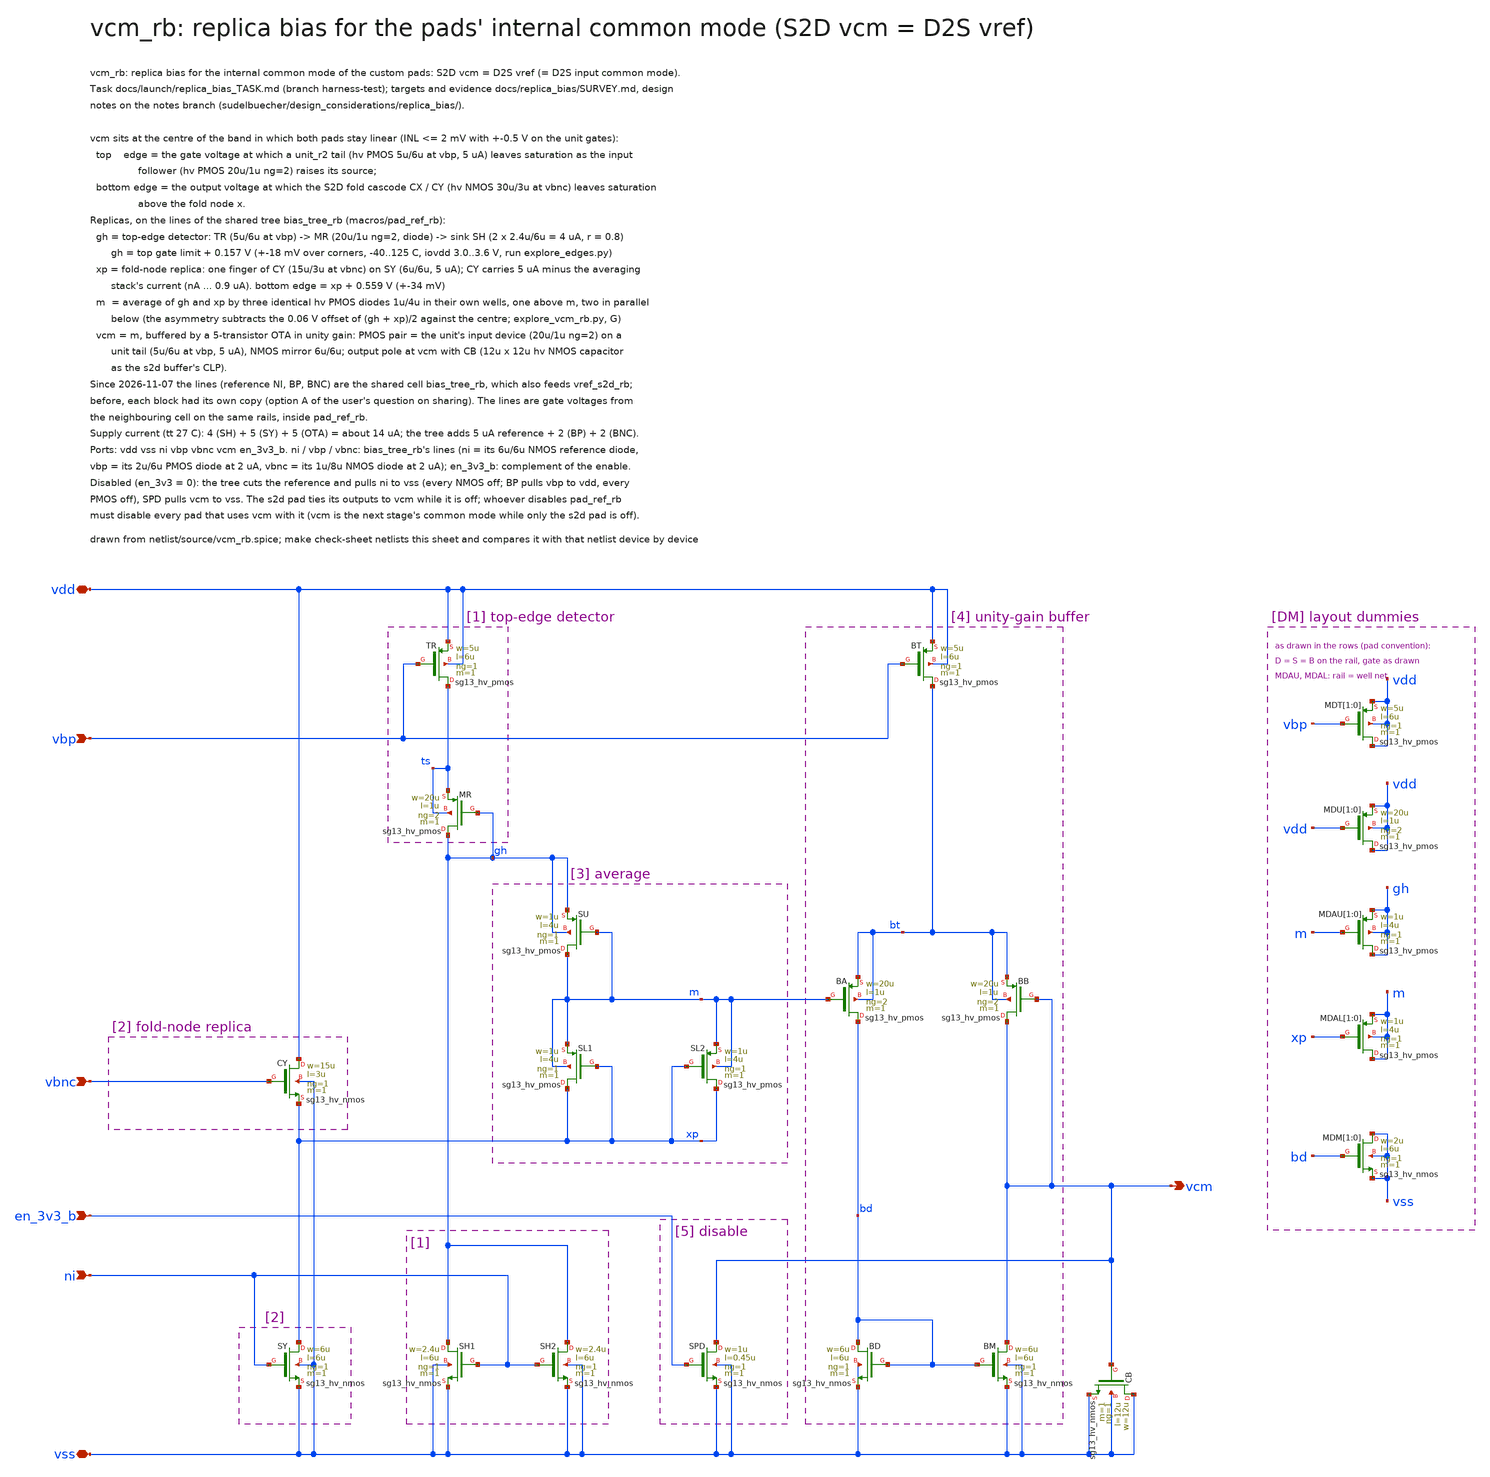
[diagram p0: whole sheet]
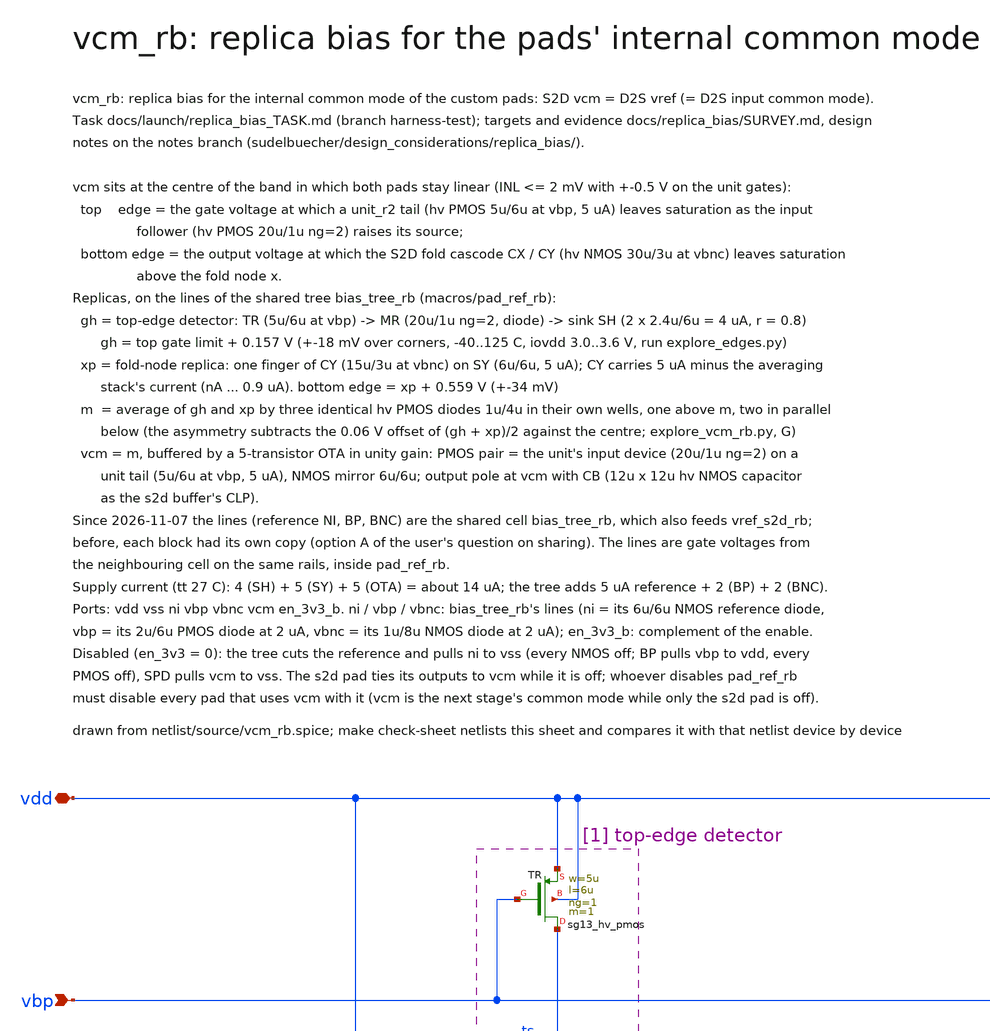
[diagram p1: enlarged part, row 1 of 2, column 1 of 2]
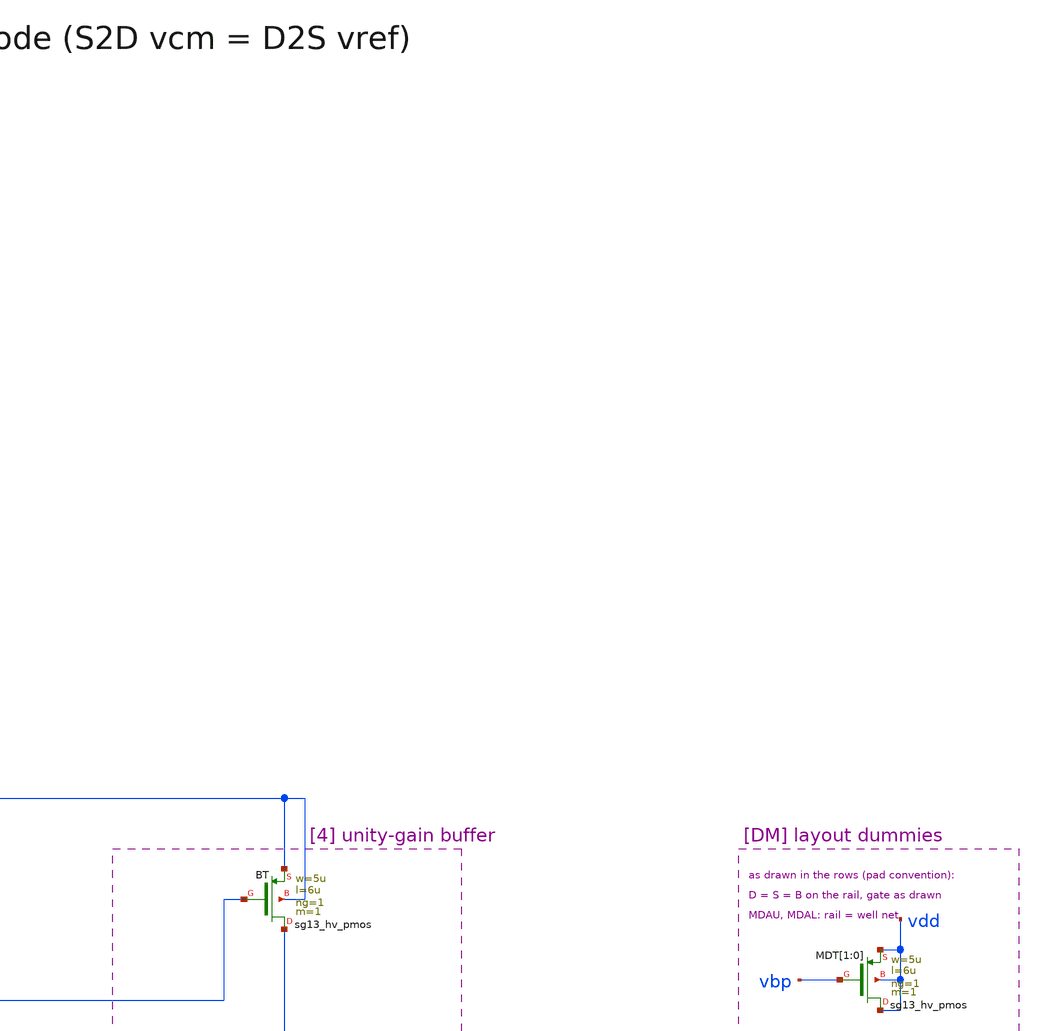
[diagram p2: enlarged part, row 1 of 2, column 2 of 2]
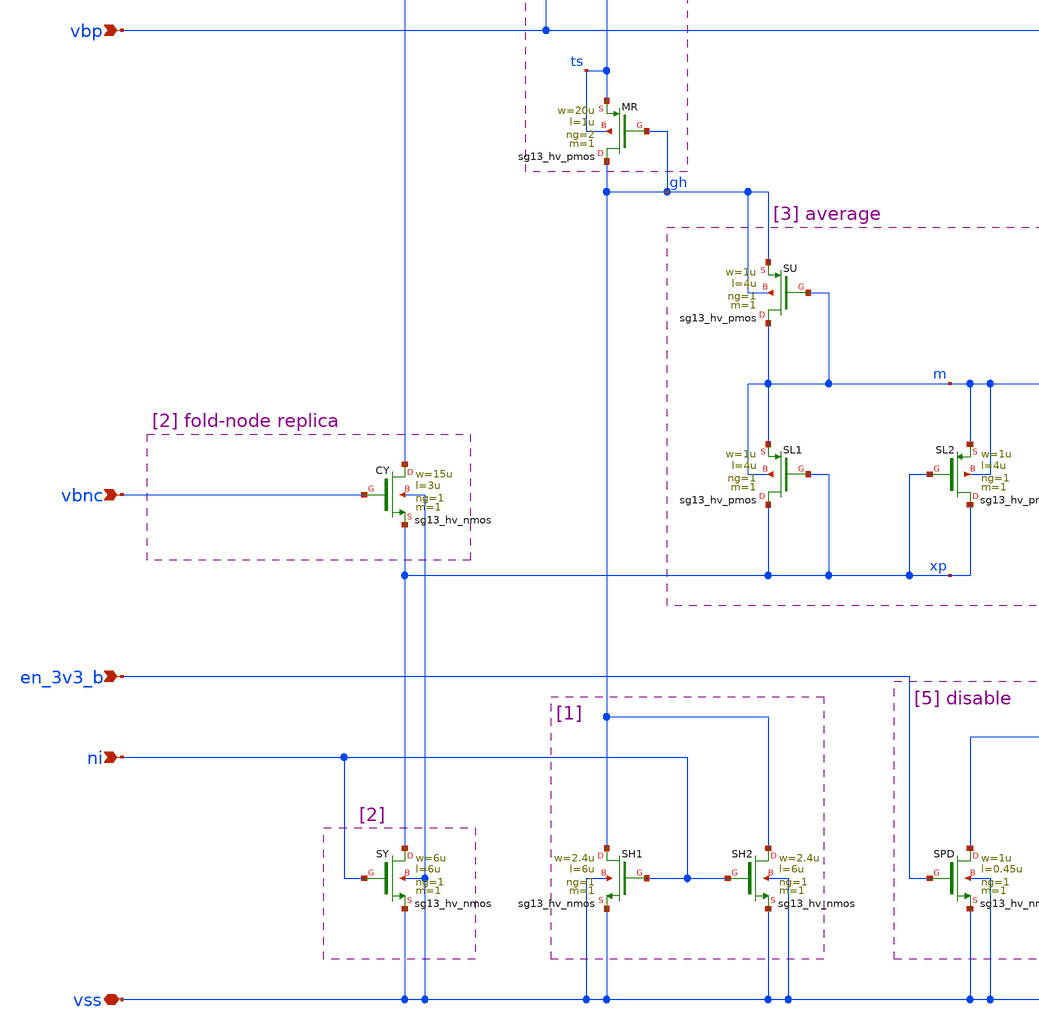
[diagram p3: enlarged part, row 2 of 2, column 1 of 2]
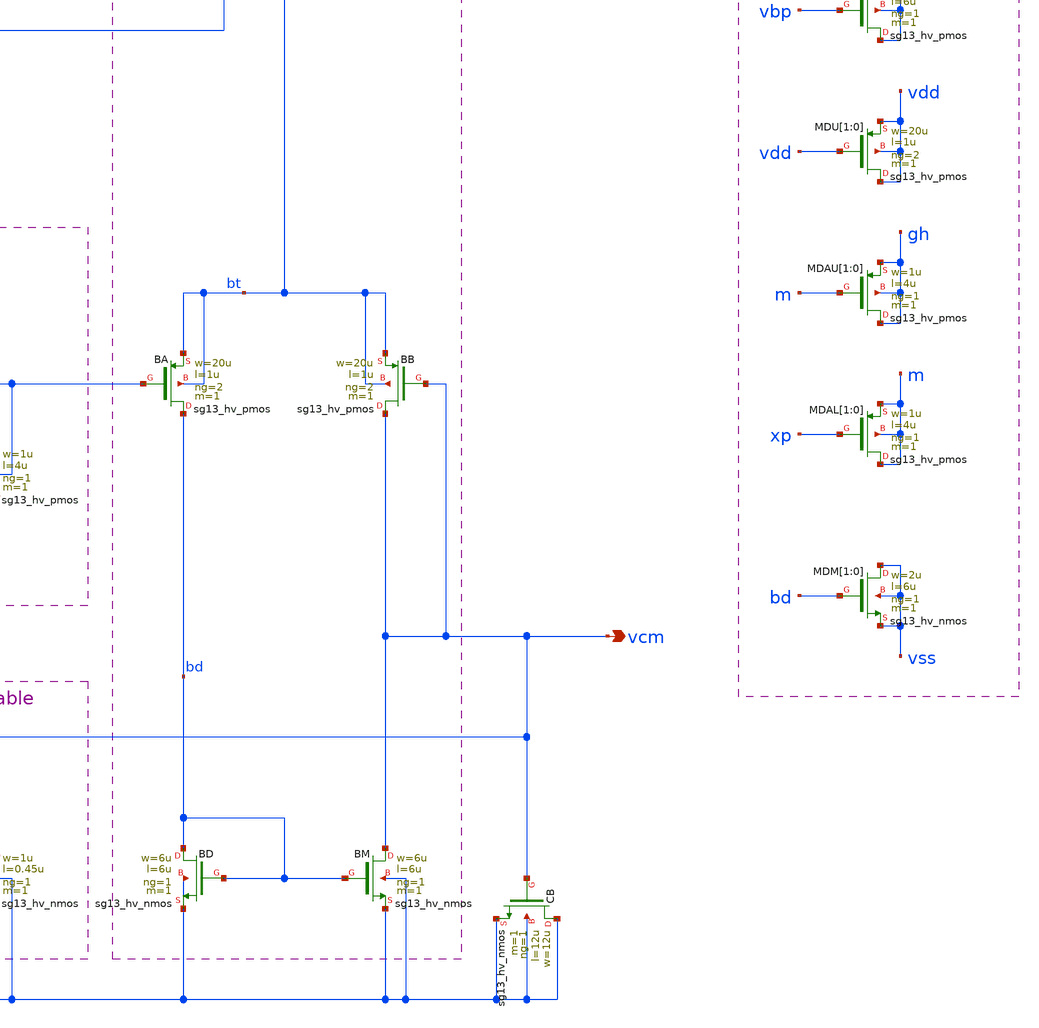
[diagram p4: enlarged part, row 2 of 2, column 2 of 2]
** sch_path: macros/vcm_rb/schematic/xschem/vcm_rb.sch
**.subckt vcm_rb vdd vss ni vbp vbnc vcm en_3v3_b
*.iopin vdd
*.iopin vss
*.ipin ni
*.ipin vbp
*.ipin vbnc
*.opin vcm
*.ipin en_3v3_b
XTR ts vbp vdd vdd sg13_hv_pmos w=5u l=6u ng=1 m=1 mm_ok=1
XMR gh gh ts ts sg13_hv_pmos w=20u l=1u ng=2 m=1 mm_ok=1
XSH1 gh ni vss vss sg13_hv_nmos w=2.4u l=6u ng=1 m=1 mm_ok=1
XSH2 gh ni vss vss sg13_hv_nmos w=2.4u l=6u ng=1 m=1 mm_ok=1
XCY vdd vbnc xp vss sg13_hv_nmos w=15u l=3u ng=1 m=1 mm_ok=1
XSY xp ni vss vss sg13_hv_nmos w=6u l=6u ng=1 m=1 mm_ok=1
XSU m m gh gh sg13_hv_pmos w=1u l=4u ng=1 m=1 mm_ok=1
XSL1 xp xp m m sg13_hv_pmos w=1u l=4u ng=1 m=1 mm_ok=1
XSL2 xp xp m m sg13_hv_pmos w=1u l=4u ng=1 m=1 mm_ok=1
XBT bt vbp vdd vdd sg13_hv_pmos w=5u l=6u ng=1 m=1 mm_ok=1
XBA bd m bt bt sg13_hv_pmos w=20u l=1u ng=2 m=1 mm_ok=1
XBB vcm vcm bt bt sg13_hv_pmos w=20u l=1u ng=2 m=1 mm_ok=1
XBD bd bd vss vss sg13_hv_nmos w=6u l=6u ng=1 m=1 mm_ok=1
XBM vcm bd vss vss sg13_hv_nmos w=6u l=6u ng=1 m=1 mm_ok=1
XCB vss vcm vss vss sg13_hv_nmos w=12u l=12u ng=1 m=1 mm_ok=1
XSPD vcm en_3v3_b vss vss sg13_hv_nmos w=1u l=0.45u ng=1 m=1 mm_ok=1
XMDT[1] vdd vbp vdd vdd sg13_hv_pmos w=5u l=6u ng=1 m=1 mm_ok=1
XMDT[0] vdd vbp vdd vdd sg13_hv_pmos w=5u l=6u ng=1 m=1 mm_ok=1
XMDU[1] vdd vdd vdd vdd sg13_hv_pmos w=20u l=1u ng=2 m=1 mm_ok=1
XMDU[0] vdd vdd vdd vdd sg13_hv_pmos w=20u l=1u ng=2 m=1 mm_ok=1
XMDAU[1] gh m gh gh sg13_hv_pmos w=1u l=4u ng=1 m=1 mm_ok=1
XMDAU[0] gh m gh gh sg13_hv_pmos w=1u l=4u ng=1 m=1 mm_ok=1
XMDAL[1] m xp m m sg13_hv_pmos w=1u l=4u ng=1 m=1 mm_ok=1
XMDAL[0] m xp m m sg13_hv_pmos w=1u l=4u ng=1 m=1 mm_ok=1
XMDM[1] vss bd vss vss sg13_hv_nmos w=2u l=6u ng=1 m=1 mm_ok=1
XMDM[0] vss bd vss vss sg13_hv_nmos w=2u l=6u ng=1 m=1 mm_ok=1
**.ends
.end
